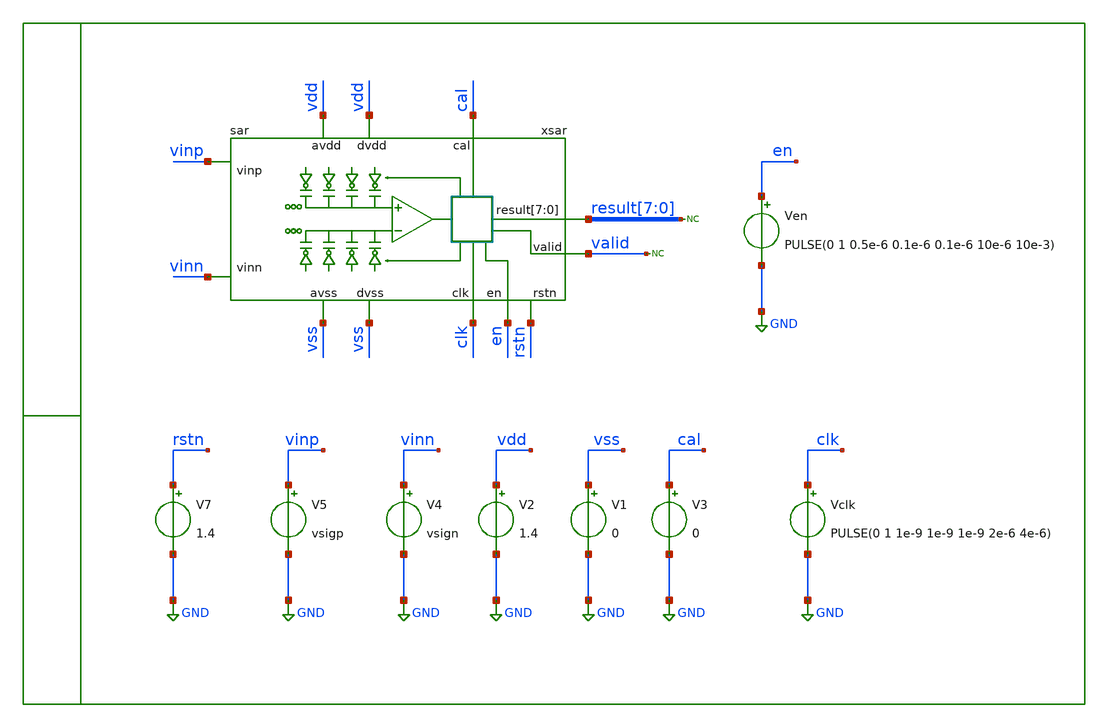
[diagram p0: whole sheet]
** sch_path: xschem/tb/sar/tr_sar.sch
**.subckt tr_sar
V1 vss GND 0
V2 vdd GND 1.4
V4 vinn GND vsign
V5 vinp GND vsigp
Vclk clk GND PULSE(0 1 1e-9 1e-9 1e-9 2e-6 4e-6)
Ven en GND PULSE(0 1 0.5e-6 0.1e-6 0.1e-6 10e-6 10e-3)
* noconn valid
V3 cal GND 0
* noconn result[7:0]
xsar vdd vdd vss result[7] result[6] result[5] result[4] result[3] result[2] result[1] result[0]
+ vinn vss clk vinp en valid cal rstn sar
V7 rstn GND 1.4
**** begin user architecture code

.include $::SKYWATER_STDCELLS/cells/inv/sky130_fd_sc_hd__inv_4.spice
.include $::SKYWATER_STDCELLS/cells/decap/sky130_fd_sc_hd__decap_8.spice
.include $::SKYWATER_STDCELLS/cells/decap/sky130_fd_sc_hd__decap_3.spice
.include $::SKYWATER_STDCELLS/cells/buf/sky130_fd_sc_hd__buf_1.spice
.include $::SKYWATER_STDCELLS/cells/inv/sky130_fd_sc_hd__inv_1.spice
.include $::SKYWATER_STDCELLS/cells/inv/sky130_fd_sc_hd__inv_2.spice
.include $::SKYWATER_STDCELLS/cells/tap/sky130_fd_sc_hd__tap_2.spice
 .options method trap
*.options method gear
.options gmin 1e-15
.options abstol 1e-15
.options reltol 0.0001
.options vntol 0.1e-6
.options warn 1

.param MC_SWITCH=0
.param vin=1
.param vcm=0.7
.param vsigp="{vcm + vin/2}"
.param vsign="{vcm - vin/2}"

.tran 100e-9 48e-6

.control

run

meas tran d0 find v(xsar.res0) at=47e-6
meas tran d1 find v(xsar.res1) at=47e-6
meas tran d2 find v(xsar.res2) at=47e-6
meas tran d3 find v(xsar.res3) at=47e-6
meas tran d4 find v(xsar.res4) at=47e-6
meas tran d5 find v(xsar.res5) at=47e-6
meas tran d6 find v(xsar.res6) at=47e-6
meas tran d7 find v(xsar.res7) at=47e-6

* meas tran d0 find v(xsar.result0) at=47e-6
* meas tran d1 find v(xsar.result1) at=47e-6
* meas tran d2 find v(xsar.result2) at=47e-6
* meas tran d3 find v(xsar.result3) at=47e-6
* meas tran d4 find v(xsar.result4) at=47e-6
* meas tran d5 find v(xsar.result5) at=47e-6
* meas tran d6 find v(xsar.result6) at=47e-6
* meas tran d7 find v(xsar.result7) at=47e-6

meas tran vpmax max xsar.vp
meas tran vpmin min xsar.vp
meas tran vpend find v(xsar.vp) at=39e-6

meas tran vnmax max xsar.vn
meas tran vnmin min xsar.vn
meas tran vnend find v(xsar.vn) at=39e-6

print d0
print d1
print d2
print d3
print d4
print d5
print d6
print d7

print vpmax
print vpmin

print vnmax
print vnmin

print vpend
print vnend

.endc
 * FET CORNERS
.include $::SKYWATER_MODELS/corners/tt.spice
*.include $::SKYWATER_MODELS/corners/ff.spice
*.include $::SKYWATER_MODELS/corners/ss.spice
*.include $::SKYWATER_MODELS/corners/sf.spice
*.include $::SKYWATER_MODELS/corners/fs.spice

* TT + R + C
*.include $::SKYWATER_MODELS/corners/tt_rmax_cmax.spice
*.include $::SKYWATER_MODELS/corners/tt_rmin_cmin.spice
*.include $::SKYWATER_MODELS/corners/tt_rmax_cmin.spice
*.include $::SKYWATER_MODELS/corners/tt_rmin_cmax.spice

* FF + R + C
*.include $::SKYWATER_MODELS/corners/ff_rmax_cmax.spice
*.include $::SKYWATER_MODELS/corners/ff_rmin_cmin.spice
*.include $::SKYWATER_MODELS/corners/ff_rmax_cmin.spice
*.include $::SKYWATER_MODELS/corners/ff_rmin_cmax.spice


* SS + R + C
*.include $::SKYWATER_MODELS/corners/ss_rmax_cmax.spice
*.include $::SKYWATER_MODELS/corners/ss_rmin_cmin.spice
*.include $::SKYWATER_MODELS/corners/ss_rmax_cmin.spice
*.include $::SKYWATER_MODELS/corners/ss_rmin_cmax.spice

* SF + R + C
*.include $::SKYWATER_MODELS/corners/sf_rmax_cmax.spice
*.include $::SKYWATER_MODELS/corners/sf_rmin_cmin.spice
*.include $::SKYWATER_MODELS/corners/sf_rmax_cmin.spice
*.include $::SKYWATER_MODELS/corners/sf_rmin_cmax.spice

* FS + R + C
*.include $::SKYWATER_MODELS/corners/fs_rmax_cmax.spice
*.include $::SKYWATER_MODELS/corners/fs_rmin_cmin.spice
*.include $::SKYWATER_MODELS/corners/fs_rmax_cmin.spice
*.include $::SKYWATER_MODELS/corners/fs_rmin_cmax.spice
**** end user architecture code
**.ends

* expanding   symbol:  sar/sar/sar.sym # of pins=12
** sym_path: xschem/sar/sar/sar.sym
** sch_path: xschem/sar/sar/sar.sch
.subckt sar avdd dvdd dvss result[7] result[6] result[5] result[4] result[3] result[2] result[1]
+ result[0] vinn avss clk vinp en valid cal rstn
*.iopin avss
*.iopin avdd
*.iopin dvss
*.iopin dvdd
*.ipin vinp
*.ipin vinn
*.opin result[7],result[6],result[5],result[4],result[3],result[2],result[1],result[0]
*.ipin clk
*.ipin en
*.opin valid
*.ipin cal
*.ipin rstn
xlat avdd net1 outp outn comp avss latch
* noconn #net1
* noconn comp
**** begin user architecture code
.include $::DESIGN_PATH/sar/control/cmos_cells_digital.sp
.include $::DESIGN_PATH/sar/control/sar_logic.sp

**** end user architecture code
* noconn sample
* noconn ctln[7:0]
* noconn ctlp[7:0]
* noconn trim[4:0]
* noconn trimb[4:0]
* noconn result[7:0]
* noconn valid
* noconn clkc
* noconn clk
* noconn en
* noconn cal
xdn vn sample avdd avss vinn ctln[7] ctln[6] ctln[5] ctln[4] ctln[3] ctln[2] ctln[1] ctln[0] avss
+ dac
xdp vp sample avdd avss vinp ctlp[7] ctlp[6] ctlp[5] ctlp[4] ctlp[3] ctlp[2] ctlp[1] ctlp[0] avdd
+ dac
xcom avss avdd clkc outp vp outn vn trim[4] trim[3] trim[2] trim[1] trim[0] trimb[4] trimb[3]
+ trimb[2] trimb[1] trimb[0] comparator
* noconn rstn
**** begin user architecture code
Xuut dclk drstn den dcomp dcal dvalid dres0 dres1 dres2 dres3 dres4 dres5 dres6 dres7 dsamp dctlp0
+ dctlp1 dctlp2 dctlp3 dctlp4 dctlp5 dctlp6 dctlp7 dctln0 dctln1 dctln2 dctln3 dctln4 dctln5 dctln6 dctln7
+ dtrim0 dtrim1 dtrim2 dtrim3 dtrim4 dtrimb0 dtrimb1 dtrimb2 dtrimb3 dtrimb4 dclkc sar_logic

.model adc_buff adc_bridge(in_low = 0.2 in_high=0.8)
.model dac_buff dac_bridge(out_high = 1.2)

Aad [clk rstn en comp cal] [dclk drstn den dcomp dcal] adc_buff
Ada [dctlp0 dctlp1 dctlp2 dctlp3 dctlp4 dctlp5 dctlp6 dctlp7 dctln0 dctln1 dctln2 dctln3 dctln4
+ dctln5 dctln6 dctln7 dres0 dres1 dres2 dres3 dres4 dres5 dres6 dres7 dsamp dclkc] [ctlp_0_ ctlp_1_ ctlp_2_
+ ctlp_3_ ctlp_4_ ctlp_5_ ctlp_6_ ctlp_7_ ctln_0_ ctln_1_ ctln_2_ ctln_3_ ctln_4_ ctln_5_ ctln_6_ ctln_7_
+ res0 res1 res2 res3 res4 res5 res6 res7 sample clkc] dac_buff
Ada2 [dtrim4 dtrim3 dtrim2 dtrim1 dtrim0 dtrimb4 dtrimb3 dtrimb2 dtrimb1 dtrimb0] [trim_4_ trim_3_
+ trim_2_ trim_1_ trim_0_ trimb_4_ trimb_3_ trimb_2_ trimb_1_ trimb_0_ ] dac_buff

**** end user architecture code
.ends


* expanding   symbol:  sar/dac/dac.sym # of pins=7
** sym_path: xschem/sar/dac/dac.sym
** sch_path: xschem/sar/dac/dac.sch
.subckt dac out sample vdd vss vin ctl[7] ctl[6] ctl[5] ctl[4] ctl[3] ctl[2] ctl[1] ctl[0] dum
*.ipin vin
*.ipin sample
*.opin out
*.ipin ctl[7],ctl[6],ctl[5],ctl[4],ctl[3],ctl[2],ctl[1],ctl[0]
*.ipin dum
*.iopin vdd
*.iopin vss
xca out n6 n0 n5 n4 n2 ndum n3 n1 n7 carray
xswt[3] out sample vss vdd vin sw_top
xswt[2] out sample vss vdd vin sw_top
xswt[1] out sample vss vdd vin sw_top
xswt[0] out sample vss vdd vin sw_top
xi6 ctl[6] vss vss vdd vdd n6 sky130_fd_sc_hd__inv_2
xi5 ctl[5] vss vss vdd vdd n5 sky130_fd_sc_hd__inv_2
xi4 ctl[4] vss vss vdd vdd n4 sky130_fd_sc_hd__inv_2
xi3 ctl[3] vss vss vdd vdd n3 sky130_fd_sc_hd__inv_2
xi2 ctl[2] vss vss vdd vdd n2 sky130_fd_sc_hd__inv_2
xi1 ctl[1] vss vss vdd vdd n1 sky130_fd_sc_hd__inv_2
xi0 ctl[0] vss vss vdd vdd n0 sky130_fd_sc_hd__inv_2
xidum dum vss vss vdd vdd ndum sky130_fd_sc_hd__inv_2
xi7 ctl[7] vss vss vdd vdd n7 sky130_fd_sc_hd__inv_2
x2[2] vss vss vdd vdd sky130_fd_sc_hd__tap_2
x2[1] vss vss vdd vdd sky130_fd_sc_hd__tap_2
x2[0] vss vss vdd vdd sky130_fd_sc_hd__tap_2
.ends


* expanding   symbol:  sar/comparator/comparator.sym # of pins=9
** sym_path: sar/comparator/comparator.sym
** sch_path: sar/comparator/comparator.sch
.subckt comparator vss vdd clk outp vp outn vn trim[4] trim[3] trim[2] trim[1] trim[0] trimb[4]
+ trimb[3] trimb[2] trimb[1] trimb[0]
*.ipin vn
*.ipin vp
*.ipin clk
*.iopin vdd
*.iopin vss
*.opin outp
*.opin outn
*.ipin trim[4],trim[3],trim[2],trim[1],trim[0]
*.ipin trimb[4],trimb[3],trimb[2],trimb[1],trimb[0]
XMdiff diff clk vss vss sky130_fd_pr__nfet_01v8 L=0.3 W=1 nf=1 ad='int((nf+1)/2) * W/nf * 0.29' as='int((nf+2)/2) * W/nf * 0.29'
+ pd='2*int((nf+1)/2) * (W/nf + 0.29)' ps='2*int((nf+2)/2) * (W/nf + 0.29)' nrd='0.29 / W' nrs='0.29 / W'
+ sa=0 sb=0 sd=0 mult=2 m=2
XMinn in vn diff vss sky130_fd_pr__nfet_01v8 L=0.3 W=1 nf=1 ad='int((nf+1)/2) * W/nf * 0.29' as='int((nf+2)/2) * W/nf * 0.29'
+ pd='2*int((nf+1)/2) * (W/nf + 0.29)' ps='2*int((nf+2)/2) * (W/nf + 0.29)' nrd='0.29 / W' nrs='0.29 / W'
+ sa=0 sb=0 sd=0 mult=1 m=1
XMinp ip vp diff vss sky130_fd_pr__nfet_01v8 L=0.3 W=1 nf=1 ad='int((nf+1)/2) * W/nf * 0.29' as='int((nf+2)/2) * W/nf * 0.29'
+ pd='2*int((nf+1)/2) * (W/nf + 0.29)' ps='2*int((nf+2)/2) * (W/nf + 0.29)' nrd='0.29 / W' nrs='0.29 / W'
+ sa=0 sb=0 sd=0 mult=1 m=1
XMl4 outp outn vdd vdd sky130_fd_pr__pfet_01v8 L=0.3 W=1 nf=1 ad='int((nf+1)/2) * W/nf * 0.29' as='int((nf+2)/2) * W/nf * 0.29'
+ pd='2*int((nf+1)/2) * (W/nf + 0.29)' ps='2*int((nf+2)/2) * (W/nf + 0.29)' nrd='0.29 / W' nrs='0.29 / W'
+ sa=0 sb=0 sd=0 mult=1 m=1
XMl3 outn outp vdd vdd sky130_fd_pr__pfet_01v8 L=0.3 W=1 nf=1 ad='int((nf+1)/2) * W/nf * 0.29' as='int((nf+2)/2) * W/nf * 0.29'
+ pd='2*int((nf+1)/2) * (W/nf + 0.29)' ps='2*int((nf+2)/2) * (W/nf + 0.29)' nrd='0.29 / W' nrs='0.29 / W'
+ sa=0 sb=0 sd=0 mult=1 m=1
XM3 outp clk vdd vdd sky130_fd_pr__pfet_01v8 L=0.3 W=1 nf=1 ad='int((nf+1)/2) * W/nf * 0.29' as='int((nf+2)/2) * W/nf * 0.29'
+ pd='2*int((nf+1)/2) * (W/nf + 0.29)' ps='2*int((nf+2)/2) * (W/nf + 0.29)' nrd='0.29 / W' nrs='0.29 / W'
+ sa=0 sb=0 sd=0 mult=1 m=1
XM2 outn clk vdd vdd sky130_fd_pr__pfet_01v8 L=0.3 W=1 nf=1 ad='int((nf+1)/2) * W/nf * 0.29' as='int((nf+2)/2) * W/nf * 0.29'
+ pd='2*int((nf+1)/2) * (W/nf + 0.29)' ps='2*int((nf+2)/2) * (W/nf + 0.29)' nrd='0.29 / W' nrs='0.29 / W'
+ sa=0 sb=0 sd=0 mult=1 m=1
XMl1 outn outp in vss sky130_fd_pr__nfet_01v8 L=0.3 W=1 nf=1 ad='int((nf+1)/2) * W/nf * 0.29' as='int((nf+2)/2) * W/nf * 0.29'
+ pd='2*int((nf+1)/2) * (W/nf + 0.29)' ps='2*int((nf+2)/2) * (W/nf + 0.29)' nrd='0.29 / W' nrs='0.29 / W'
+ sa=0 sb=0 sd=0 mult=1 m=1
XMl2 outp outn ip vss sky130_fd_pr__nfet_01v8 L=0.3 W=1 nf=1 ad='int((nf+1)/2) * W/nf * 0.29' as='int((nf+2)/2) * W/nf * 0.29'
+ pd='2*int((nf+1)/2) * (W/nf + 0.29)' ps='2*int((nf+2)/2) * (W/nf + 0.29)' nrd='0.29 / W' nrs='0.29 / W'
+ sa=0 sb=0 sd=0 mult=1 m=1
XM4 ip clk vdd vdd sky130_fd_pr__pfet_01v8 L=0.3 W=1 nf=1 ad='int((nf+1)/2) * W/nf * 0.29' as='int((nf+2)/2) * W/nf * 0.29'
+ pd='2*int((nf+1)/2) * (W/nf + 0.29)' ps='2*int((nf+2)/2) * (W/nf + 0.29)' nrd='0.29 / W' nrs='0.29 / W'
+ sa=0 sb=0 sd=0 mult=1 m=1
XM1 in clk vdd vdd sky130_fd_pr__pfet_01v8 L=0.3 W=1 nf=1 ad='int((nf+1)/2) * W/nf * 0.29' as='int((nf+2)/2) * W/nf * 0.29'
+ pd='2*int((nf+1)/2) * (W/nf + 0.29)' ps='2*int((nf+2)/2) * (W/nf + 0.29)' nrd='0.29 / W' nrs='0.29 / W'
+ sa=0 sb=0 sd=0 mult=1 m=1
x2 in trim[4] trim[3] trim[2] trim[1] trim[0] vss trim
x3 ip trimb[4] trimb[3] trimb[2] trimb[1] trimb[0] vss trim
.ends


* expanding   symbol:  sar/dac/carray.sym # of pins=10
** sym_path: xschem/sar/dac/carray.sym
** sch_path: xschem/sar/dac/carray.sch
.subckt carray top n6 n0 n5 n4 n2 ndum n3 n1 n7
*.iopin top
*.iopin n7
*.iopin n6
*.iopin n5
*.iopin n4
*.iopin n2
*.iopin n0
*.iopin ndum
*.iopin n3
*.iopin n1
xcdum top ndum unitcap
xc0 top n0 unitcap
xc1[1] top n1 unitcap
xc1[0] top n1 unitcap
xc2[3] top n2 unitcap
xc2[2] top n2 unitcap
xc2[1] top n2 unitcap
xc2[0] top n2 unitcap
xc3[7] top n3 unitcap
xc3[6] top n3 unitcap
xc3[5] top n3 unitcap
xc3[4] top n3 unitcap
xc3[3] top n3 unitcap
xc3[2] top n3 unitcap
xc3[1] top n3 unitcap
xc3[0] top n3 unitcap
xc4[15] top n4 unitcap
xc4[14] top n4 unitcap
xc4[13] top n4 unitcap
xc4[12] top n4 unitcap
xc4[11] top n4 unitcap
xc4[10] top n4 unitcap
xc4[9] top n4 unitcap
xc4[8] top n4 unitcap
xc4[7] top n4 unitcap
xc4[6] top n4 unitcap
xc4[5] top n4 unitcap
xc4[4] top n4 unitcap
xc4[3] top n4 unitcap
xc4[2] top n4 unitcap
xc4[1] top n4 unitcap
xc4[0] top n4 unitcap
xc5[31] top n5 unitcap
xc5[30] top n5 unitcap
xc5[29] top n5 unitcap
xc5[28] top n5 unitcap
xc5[27] top n5 unitcap
xc5[26] top n5 unitcap
xc5[25] top n5 unitcap
xc5[24] top n5 unitcap
xc5[23] top n5 unitcap
xc5[22] top n5 unitcap
xc5[21] top n5 unitcap
xc5[20] top n5 unitcap
xc5[19] top n5 unitcap
xc5[18] top n5 unitcap
xc5[17] top n5 unitcap
xc5[16] top n5 unitcap
xc5[15] top n5 unitcap
xc5[14] top n5 unitcap
xc5[13] top n5 unitcap
xc5[12] top n5 unitcap
xc5[11] top n5 unitcap
xc5[10] top n5 unitcap
xc5[9] top n5 unitcap
xc5[8] top n5 unitcap
xc5[7] top n5 unitcap
xc5[6] top n5 unitcap
xc5[5] top n5 unitcap
xc5[4] top n5 unitcap
xc5[3] top n5 unitcap
xc5[2] top n5 unitcap
xc5[1] top n5 unitcap
xc5[0] top n5 unitcap
xc6[63] top n6 unitcap
xc6[62] top n6 unitcap
xc6[61] top n6 unitcap
xc6[60] top n6 unitcap
xc6[59] top n6 unitcap
xc6[58] top n6 unitcap
xc6[57] top n6 unitcap
xc6[56] top n6 unitcap
xc6[55] top n6 unitcap
xc6[54] top n6 unitcap
xc6[53] top n6 unitcap
xc6[52] top n6 unitcap
xc6[51] top n6 unitcap
xc6[50] top n6 unitcap
xc6[49] top n6 unitcap
xc6[48] top n6 unitcap
xc6[47] top n6 unitcap
xc6[46] top n6 unitcap
xc6[45] top n6 unitcap
xc6[44] top n6 unitcap
xc6[43] top n6 unitcap
xc6[42] top n6 unitcap
xc6[41] top n6 unitcap
xc6[40] top n6 unitcap
xc6[39] top n6 unitcap
xc6[38] top n6 unitcap
xc6[37] top n6 unitcap
xc6[36] top n6 unitcap
xc6[35] top n6 unitcap
xc6[34] top n6 unitcap
xc6[33] top n6 unitcap
xc6[32] top n6 unitcap
xc6[31] top n6 unitcap
xc6[30] top n6 unitcap
xc6[29] top n6 unitcap
xc6[28] top n6 unitcap
xc6[27] top n6 unitcap
xc6[26] top n6 unitcap
xc6[25] top n6 unitcap
xc6[24] top n6 unitcap
xc6[23] top n6 unitcap
xc6[22] top n6 unitcap
xc6[21] top n6 unitcap
xc6[20] top n6 unitcap
xc6[19] top n6 unitcap
xc6[18] top n6 unitcap
xc6[17] top n6 unitcap
xc6[16] top n6 unitcap
xc6[15] top n6 unitcap
xc6[14] top n6 unitcap
xc6[13] top n6 unitcap
xc6[12] top n6 unitcap
xc6[11] top n6 unitcap
xc6[10] top n6 unitcap
xc6[9] top n6 unitcap
xc6[8] top n6 unitcap
xc6[7] top n6 unitcap
xc6[6] top n6 unitcap
xc6[5] top n6 unitcap
xc6[4] top n6 unitcap
xc6[3] top n6 unitcap
xc6[2] top n6 unitcap
xc6[1] top n6 unitcap
xc6[0] top n6 unitcap
xc7[127] top n7 unitcap
xc7[126] top n7 unitcap
xc7[125] top n7 unitcap
xc7[124] top n7 unitcap
xc7[123] top n7 unitcap
xc7[122] top n7 unitcap
xc7[121] top n7 unitcap
xc7[120] top n7 unitcap
xc7[119] top n7 unitcap
xc7[118] top n7 unitcap
xc7[117] top n7 unitcap
xc7[116] top n7 unitcap
xc7[115] top n7 unitcap
xc7[114] top n7 unitcap
xc7[113] top n7 unitcap
xc7[112] top n7 unitcap
xc7[111] top n7 unitcap
xc7[110] top n7 unitcap
xc7[109] top n7 unitcap
xc7[108] top n7 unitcap
xc7[107] top n7 unitcap
xc7[106] top n7 unitcap
xc7[105] top n7 unitcap
xc7[104] top n7 unitcap
xc7[103] top n7 unitcap
xc7[102] top n7 unitcap
xc7[101] top n7 unitcap
xc7[100] top n7 unitcap
xc7[99] top n7 unitcap
xc7[98] top n7 unitcap
xc7[97] top n7 unitcap
xc7[96] top n7 unitcap
xc7[95] top n7 unitcap
xc7[94] top n7 unitcap
xc7[93] top n7 unitcap
xc7[92] top n7 unitcap
xc7[91] top n7 unitcap
xc7[90] top n7 unitcap
xc7[89] top n7 unitcap
xc7[88] top n7 unitcap
xc7[87] top n7 unitcap
xc7[86] top n7 unitcap
xc7[85] top n7 unitcap
xc7[84] top n7 unitcap
xc7[83] top n7 unitcap
xc7[82] top n7 unitcap
xc7[81] top n7 unitcap
xc7[80] top n7 unitcap
xc7[79] top n7 unitcap
xc7[78] top n7 unitcap
xc7[77] top n7 unitcap
xc7[76] top n7 unitcap
xc7[75] top n7 unitcap
xc7[74] top n7 unitcap
xc7[73] top n7 unitcap
xc7[72] top n7 unitcap
xc7[71] top n7 unitcap
xc7[70] top n7 unitcap
xc7[69] top n7 unitcap
xc7[68] top n7 unitcap
xc7[67] top n7 unitcap
xc7[66] top n7 unitcap
xc7[65] top n7 unitcap
xc7[64] top n7 unitcap
xc7[63] top n7 unitcap
xc7[62] top n7 unitcap
xc7[61] top n7 unitcap
xc7[60] top n7 unitcap
xc7[59] top n7 unitcap
xc7[58] top n7 unitcap
xc7[57] top n7 unitcap
xc7[56] top n7 unitcap
xc7[55] top n7 unitcap
xc7[54] top n7 unitcap
xc7[53] top n7 unitcap
xc7[52] top n7 unitcap
xc7[51] top n7 unitcap
xc7[50] top n7 unitcap
xc7[49] top n7 unitcap
xc7[48] top n7 unitcap
xc7[47] top n7 unitcap
xc7[46] top n7 unitcap
xc7[45] top n7 unitcap
xc7[44] top n7 unitcap
xc7[43] top n7 unitcap
xc7[42] top n7 unitcap
xc7[41] top n7 unitcap
xc7[40] top n7 unitcap
xc7[39] top n7 unitcap
xc7[38] top n7 unitcap
xc7[37] top n7 unitcap
xc7[36] top n7 unitcap
xc7[35] top n7 unitcap
xc7[34] top n7 unitcap
xc7[33] top n7 unitcap
xc7[32] top n7 unitcap
xc7[31] top n7 unitcap
xc7[30] top n7 unitcap
xc7[29] top n7 unitcap
xc7[28] top n7 unitcap
xc7[27] top n7 unitcap
xc7[26] top n7 unitcap
xc7[25] top n7 unitcap
xc7[24] top n7 unitcap
xc7[23] top n7 unitcap
xc7[22] top n7 unitcap
xc7[21] top n7 unitcap
xc7[20] top n7 unitcap
xc7[19] top n7 unitcap
xc7[18] top n7 unitcap
xc7[17] top n7 unitcap
xc7[16] top n7 unitcap
xc7[15] top n7 unitcap
xc7[14] top n7 unitcap
xc7[13] top n7 unitcap
xc7[12] top n7 unitcap
xc7[11] top n7 unitcap
xc7[10] top n7 unitcap
xc7[9] top n7 unitcap
xc7[8] top n7 unitcap
xc7[7] top n7 unitcap
xc7[6] top n7 unitcap
xc7[5] top n7 unitcap
xc7[4] top n7 unitcap
xc7[3] top n7 unitcap
xc7[2] top n7 unitcap
xc7[1] top n7 unitcap
xc7[0] top n7 unitcap
xdummy[83] top dum_bot[83] unitcap
xdummy[82] top dum_bot[82] unitcap
xdummy[81] top dum_bot[81] unitcap
xdummy[80] top dum_bot[80] unitcap
xdummy[79] top dum_bot[79] unitcap
xdummy[78] top dum_bot[78] unitcap
xdummy[77] top dum_bot[77] unitcap
xdummy[76] top dum_bot[76] unitcap
xdummy[75] top dum_bot[75] unitcap
xdummy[74] top dum_bot[74] unitcap
xdummy[73] top dum_bot[73] unitcap
xdummy[72] top dum_bot[72] unitcap
xdummy[71] top dum_bot[71] unitcap
xdummy[70] top dum_bot[70] unitcap
xdummy[69] top dum_bot[69] unitcap
xdummy[68] top dum_bot[68] unitcap
xdummy[67] top dum_bot[67] unitcap
xdummy[66] top dum_bot[66] unitcap
xdummy[65] top dum_bot[65] unitcap
xdummy[64] top dum_bot[64] unitcap
xdummy[63] top dum_bot[63] unitcap
xdummy[62] top dum_bot[62] unitcap
xdummy[61] top dum_bot[61] unitcap
xdummy[60] top dum_bot[60] unitcap
xdummy[59] top dum_bot[59] unitcap
xdummy[58] top dum_bot[58] unitcap
xdummy[57] top dum_bot[57] unitcap
xdummy[56] top dum_bot[56] unitcap
xdummy[55] top dum_bot[55] unitcap
xdummy[54] top dum_bot[54] unitcap
xdummy[53] top dum_bot[53] unitcap
xdummy[52] top dum_bot[52] unitcap
xdummy[51] top dum_bot[51] unitcap
xdummy[50] top dum_bot[50] unitcap
xdummy[49] top dum_bot[49] unitcap
xdummy[48] top dum_bot[48] unitcap
xdummy[47] top dum_bot[47] unitcap
xdummy[46] top dum_bot[46] unitcap
xdummy[45] top dum_bot[45] unitcap
xdummy[44] top dum_bot[44] unitcap
xdummy[43] top dum_bot[43] unitcap
xdummy[42] top dum_bot[42] unitcap
xdummy[41] top dum_bot[41] unitcap
xdummy[40] top dum_bot[40] unitcap
xdummy[39] top dum_bot[39] unitcap
xdummy[38] top dum_bot[38] unitcap
xdummy[37] top dum_bot[37] unitcap
xdummy[36] top dum_bot[36] unitcap
xdummy[35] top dum_bot[35] unitcap
xdummy[34] top dum_bot[34] unitcap
xdummy[33] top dum_bot[33] unitcap
xdummy[32] top dum_bot[32] unitcap
xdummy[31] top dum_bot[31] unitcap
xdummy[30] top dum_bot[30] unitcap
xdummy[29] top dum_bot[29] unitcap
xdummy[28] top dum_bot[28] unitcap
xdummy[27] top dum_bot[27] unitcap
xdummy[26] top dum_bot[26] unitcap
xdummy[25] top dum_bot[25] unitcap
xdummy[24] top dum_bot[24] unitcap
xdummy[23] top dum_bot[23] unitcap
xdummy[22] top dum_bot[22] unitcap
xdummy[21] top dum_bot[21] unitcap
xdummy[20] top dum_bot[20] unitcap
xdummy[19] top dum_bot[19] unitcap
xdummy[18] top dum_bot[18] unitcap
xdummy[17] top dum_bot[17] unitcap
xdummy[16] top dum_bot[16] unitcap
xdummy[15] top dum_bot[15] unitcap
xdummy[14] top dum_bot[14] unitcap
xdummy[13] top dum_bot[13] unitcap
xdummy[12] top dum_bot[12] unitcap
xdummy[11] top dum_bot[11] unitcap
xdummy[10] top dum_bot[10] unitcap
xdummy[9] top dum_bot[9] unitcap
xdummy[8] top dum_bot[8] unitcap
xdummy[7] top dum_bot[7] unitcap
xdummy[6] top dum_bot[6] unitcap
xdummy[5] top dum_bot[5] unitcap
xdummy[4] top dum_bot[4] unitcap
xdummy[3] top dum_bot[3] unitcap
xdummy[2] top dum_bot[2] unitcap
xdummy[1] top dum_bot[1] unitcap
xdummy[0] top dum_bot[0] unitcap
* noconn dum_bot[83:0]
.ends


* expanding   symbol:  sar/sw/sw_top.sym # of pins=5
** sym_path: sar/sw/sw_top.sym
** sch_path: sar/sw/sw_top.sch
.subckt sw_top out en vss vdd in
*.iopin out
*.ipin en
*.iopin vss
*.iopin vdd
*.iopin in
XM3 in enb out vdd sky130_fd_pr__pfet_01v8 L=0.3 W=1 nf=1 ad='int((nf+1)/2) * W/nf * 0.29' as='int((nf+2)/2) * W/nf * 0.29'
+ pd='2*int((nf+1)/2) * (W/nf + 0.29)' ps='2*int((nf+2)/2) * (W/nf + 0.29)' nrd='0.29 / W' nrs='0.29 / W'
+ sa=0 sb=0 sd=0 mult=10 m=10
XM4 in en_buf out vss sky130_fd_pr__nfet_01v8 L=0.3 W=1 nf=1 ad='int((nf+1)/2) * W/nf * 0.29' as='int((nf+2)/2) * W/nf * 0.29'
+ pd='2*int((nf+1)/2) * (W/nf + 0.29)' ps='2*int((nf+2)/2) * (W/nf + 0.29)' nrd='0.29 / W' nrs='0.29 / W'
+ sa=0 sb=0 sd=0 mult=10 m=10
x2 vss vss vdd vdd sky130_fd_sc_hd__decap_8
x3 en vss vss vdd vdd enb sky130_fd_sc_hd__inv_4
x4 enb vss vss vdd vdd en_buf sky130_fd_sc_hd__inv_4
x5 vss vss vdd vdd sky130_fd_sc_hd__decap_3
.ends


* expanding   symbol:  sar/comparator/trim.sym # of pins=3
** sym_path: sar/comparator/trim.sym
** sch_path: sar/comparator/trim.sch
.subckt trim drain d[4] d[3] d[2] d[1] d[0] vss
*.iopin vss
*.ipin d[4],d[3],d[2],d[1],d[0]
*.opin drain
XM4[7] n4 d[4] vss vss sky130_fd_pr__nfet_01v8_lvt L=0.3 W=1 nf=1 ad='int((nf+1)/2) * W/nf * 0.29' as='int((nf+2)/2) * W/nf * 0.29'
+ pd='2*int((nf+1)/2) * (W/nf + 0.29)' ps='2*int((nf+2)/2) * (W/nf + 0.29)' nrd='0.29 / W' nrs='0.29 / W'
+ sa=0 sb=0 sd=0 mult=1 m=1
XM4[6] n4 d[4] vss vss sky130_fd_pr__nfet_01v8_lvt L=0.3 W=1 nf=1 ad='int((nf+1)/2) * W/nf * 0.29' as='int((nf+2)/2) * W/nf * 0.29'
+ pd='2*int((nf+1)/2) * (W/nf + 0.29)' ps='2*int((nf+2)/2) * (W/nf + 0.29)' nrd='0.29 / W' nrs='0.29 / W'
+ sa=0 sb=0 sd=0 mult=1 m=1
XM4[5] n4 d[4] vss vss sky130_fd_pr__nfet_01v8_lvt L=0.3 W=1 nf=1 ad='int((nf+1)/2) * W/nf * 0.29' as='int((nf+2)/2) * W/nf * 0.29'
+ pd='2*int((nf+1)/2) * (W/nf + 0.29)' ps='2*int((nf+2)/2) * (W/nf + 0.29)' nrd='0.29 / W' nrs='0.29 / W'
+ sa=0 sb=0 sd=0 mult=1 m=1
XM4[4] n4 d[4] vss vss sky130_fd_pr__nfet_01v8_lvt L=0.3 W=1 nf=1 ad='int((nf+1)/2) * W/nf * 0.29' as='int((nf+2)/2) * W/nf * 0.29'
+ pd='2*int((nf+1)/2) * (W/nf + 0.29)' ps='2*int((nf+2)/2) * (W/nf + 0.29)' nrd='0.29 / W' nrs='0.29 / W'
+ sa=0 sb=0 sd=0 mult=1 m=1
XM4[3] n4 d[4] vss vss sky130_fd_pr__nfet_01v8_lvt L=0.3 W=1 nf=1 ad='int((nf+1)/2) * W/nf * 0.29' as='int((nf+2)/2) * W/nf * 0.29'
+ pd='2*int((nf+1)/2) * (W/nf + 0.29)' ps='2*int((nf+2)/2) * (W/nf + 0.29)' nrd='0.29 / W' nrs='0.29 / W'
+ sa=0 sb=0 sd=0 mult=1 m=1
XM4[2] n4 d[4] vss vss sky130_fd_pr__nfet_01v8_lvt L=0.3 W=1 nf=1 ad='int((nf+1)/2) * W/nf * 0.29' as='int((nf+2)/2) * W/nf * 0.29'
+ pd='2*int((nf+1)/2) * (W/nf + 0.29)' ps='2*int((nf+2)/2) * (W/nf + 0.29)' nrd='0.29 / W' nrs='0.29 / W'
+ sa=0 sb=0 sd=0 mult=1 m=1
XM4[1] n4 d[4] vss vss sky130_fd_pr__nfet_01v8_lvt L=0.3 W=1 nf=1 ad='int((nf+1)/2) * W/nf * 0.29' as='int((nf+2)/2) * W/nf * 0.29'
+ pd='2*int((nf+1)/2) * (W/nf + 0.29)' ps='2*int((nf+2)/2) * (W/nf + 0.29)' nrd='0.29 / W' nrs='0.29 / W'
+ sa=0 sb=0 sd=0 mult=1 m=1
XM4[0] n4 d[4] vss vss sky130_fd_pr__nfet_01v8_lvt L=0.3 W=1 nf=1 ad='int((nf+1)/2) * W/nf * 0.29' as='int((nf+2)/2) * W/nf * 0.29'
+ pd='2*int((nf+1)/2) * (W/nf + 0.29)' ps='2*int((nf+2)/2) * (W/nf + 0.29)' nrd='0.29 / W' nrs='0.29 / W'
+ sa=0 sb=0 sd=0 mult=1 m=1
XM3[3] n3 d[3] vss vss sky130_fd_pr__nfet_01v8_lvt L=0.3 W=1 nf=1 ad='int((nf+1)/2) * W/nf * 0.29' as='int((nf+2)/2) * W/nf * 0.29'
+ pd='2*int((nf+1)/2) * (W/nf + 0.29)' ps='2*int((nf+2)/2) * (W/nf + 0.29)' nrd='0.29 / W' nrs='0.29 / W'
+ sa=0 sb=0 sd=0 mult=1 m=1
XM3[2] n3 d[3] vss vss sky130_fd_pr__nfet_01v8_lvt L=0.3 W=1 nf=1 ad='int((nf+1)/2) * W/nf * 0.29' as='int((nf+2)/2) * W/nf * 0.29'
+ pd='2*int((nf+1)/2) * (W/nf + 0.29)' ps='2*int((nf+2)/2) * (W/nf + 0.29)' nrd='0.29 / W' nrs='0.29 / W'
+ sa=0 sb=0 sd=0 mult=1 m=1
XM3[1] n3 d[3] vss vss sky130_fd_pr__nfet_01v8_lvt L=0.3 W=1 nf=1 ad='int((nf+1)/2) * W/nf * 0.29' as='int((nf+2)/2) * W/nf * 0.29'
+ pd='2*int((nf+1)/2) * (W/nf + 0.29)' ps='2*int((nf+2)/2) * (W/nf + 0.29)' nrd='0.29 / W' nrs='0.29 / W'
+ sa=0 sb=0 sd=0 mult=1 m=1
XM3[0] n3 d[3] vss vss sky130_fd_pr__nfet_01v8_lvt L=0.3 W=1 nf=1 ad='int((nf+1)/2) * W/nf * 0.29' as='int((nf+2)/2) * W/nf * 0.29'
+ pd='2*int((nf+1)/2) * (W/nf + 0.29)' ps='2*int((nf+2)/2) * (W/nf + 0.29)' nrd='0.29 / W' nrs='0.29 / W'
+ sa=0 sb=0 sd=0 mult=1 m=1
XM2[1] n2 d[2] vss vss sky130_fd_pr__nfet_01v8_lvt L=0.3 W=1 nf=1 ad='int((nf+1)/2) * W/nf * 0.29' as='int((nf+2)/2) * W/nf * 0.29'
+ pd='2*int((nf+1)/2) * (W/nf + 0.29)' ps='2*int((nf+2)/2) * (W/nf + 0.29)' nrd='0.29 / W' nrs='0.29 / W'
+ sa=0 sb=0 sd=0 mult=1 m=1
XM2[0] n2 d[2] vss vss sky130_fd_pr__nfet_01v8_lvt L=0.3 W=1 nf=1 ad='int((nf+1)/2) * W/nf * 0.29' as='int((nf+2)/2) * W/nf * 0.29'
+ pd='2*int((nf+1)/2) * (W/nf + 0.29)' ps='2*int((nf+2)/2) * (W/nf + 0.29)' nrd='0.29 / W' nrs='0.29 / W'
+ sa=0 sb=0 sd=0 mult=1 m=1
XM1 n1 d[1] vss vss sky130_fd_pr__nfet_01v8_lvt L=0.3 W=1 nf=1 ad='int((nf+1)/2) * W/nf * 0.29' as='int((nf+2)/2) * W/nf * 0.29'
+ pd='2*int((nf+1)/2) * (W/nf + 0.29)' ps='2*int((nf+2)/2) * (W/nf + 0.29)' nrd='0.29 / W' nrs='0.29 / W'
+ sa=0 sb=0 sd=0 mult=1 m=1
XM0 n0 d[0] vss vss sky130_fd_pr__nfet_01v8_lvt L=0.3 W=1 nf=1 ad='int((nf+1)/2) * W/nf * 0.29' as='int((nf+2)/2) * W/nf * 0.29'
+ pd='2*int((nf+1)/2) * (W/nf + 0.29)' ps='2*int((nf+2)/2) * (W/nf + 0.29)' nrd='0.29 / W' nrs='0.29 / W'
+ sa=0 sb=0 sd=0 mult=1 m=1
x4[7] drain n4 trimcap
x4[6] drain n4 trimcap
x4[5] drain n4 trimcap
x4[4] drain n4 trimcap
x4[3] drain n4 trimcap
x4[2] drain n4 trimcap
x4[1] drain n4 trimcap
x4[0] drain n4 trimcap
x3[3] drain n3 trimcap
x3[2] drain n3 trimcap
x3[1] drain n3 trimcap
x3[0] drain n3 trimcap
x2[1] drain n2 trimcap
x2[0] drain n2 trimcap
x1 drain n1 trimcap
x0 drain n0 trimcap
.ends


* expanding   symbol:  sar/unitcap/unitcap.sym # of pins=2
** sym_path: sar/unitcap/unitcap.sym
** sch_path: sar/unitcap/unitcap.sch
.subckt unitcap cp cn
*.iopin cp
*.iopin cn
XC1 cp cn sky130_fd_pr__cap_mim_m3_1 W=2 L=2 MF=1 m=1
.ends


* expanding   symbol:  sar/comparator/trimcap.sym # of pins=2
** sym_path: sar/comparator/trimcap.sym
** sch_path: sar/comparator/trimcap.sch
.subckt trimcap cp cn
*.iopin cp
*.iopin cn
c0 cp cn 2f m=1
.ends

.GLOBAL GND
.end
